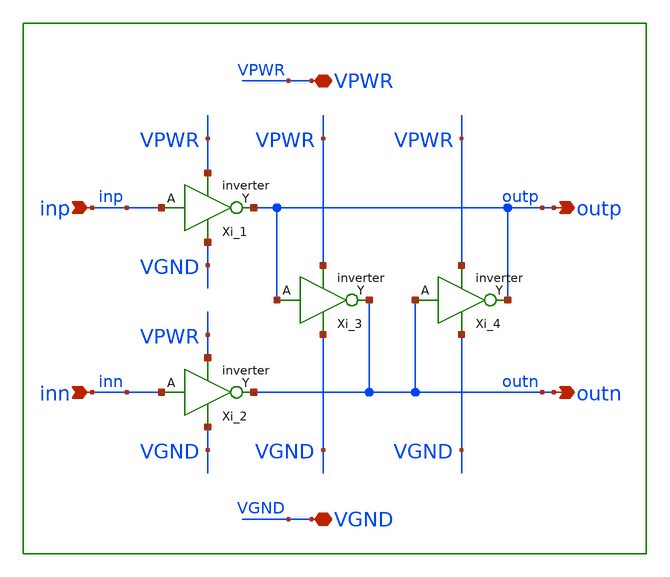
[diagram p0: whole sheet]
** sch_path: circuit_model/lib/cc_inv.sch
**.subckt cc_inv outp inn VGND outn inp VPWR
*.opin outp
*.ipin inn
*.iopin VGND
*.opin outn
*.ipin inp
*.iopin VPWR
Xi_1 inp VPWR VGND outp inverter L="L12" Wp="Wp12" Np=1 Wn="Wn12" Nn=1
Xi_3 outp VPWR VGND outn inverter L="L34" Wp="Wp34" Np=1 Wn="Wn34" Nn=1
Xi_2 inn VPWR VGND outn inverter L="L12" Wp="Wp12" Np=1 Wn="Wn12" Nn=1
Xi_4 outn VPWR VGND outp inverter L="L34" Wp="Wp34" Np=1 Wn="Wn34" Nn=1
**.ends

* expanding   symbol:  inverter.sym # of pins=4
** sym_path: circuit_model/lib/inverter.sym
** sch_path: circuit_model/lib/inverter.sch
.subckt inverter A VPWR VGND Y  L=0.15 Wp=1.2 Np=1 Wn=0.65 Nn=1
*.iopin VPWR
*.iopin VGND
*.ipin A
*.opin Y
XM1 Y A VPWR VDD sky130_fd_pr__pfet_01v8 L="L" W="Wp" nf="Np" ad='int(("Np" + 1)/2) * "Wp" / "Np" * 0.29'
+ as='int(("Np" + 2)/2) * "Wp" / "Np" * 0.29' pd='2*int(("Np" + 1)/2) * ("Wp" / "Np" + 0.29)' ps='2*int(("Np" + 2)/2) * ("Wp" / "Np" + 0.29)'
+ nrd='0.29 / "Wp" ' nrs='0.29 / "Wp" ' sa=0 sb=0 sd=0 mult=1 m=1
XM2 Y A VGND GND sky130_fd_pr__nfet_01v8 L="L" W="Wn" nf="Nn" ad='int((nf+1)/2) * W/nf * 0.29' as='int((nf+2)/2) * W/nf * 0.29'
+ pd='2*int((nf+1)/2) * (W/nf + 0.29)' ps='2*int((nf+2)/2) * (W/nf + 0.29)' nrd='0.29 / W' nrs='0.29 / W'
+ sa=0 sb=0 sd=0 mult=1 m=1
.ends

.end
